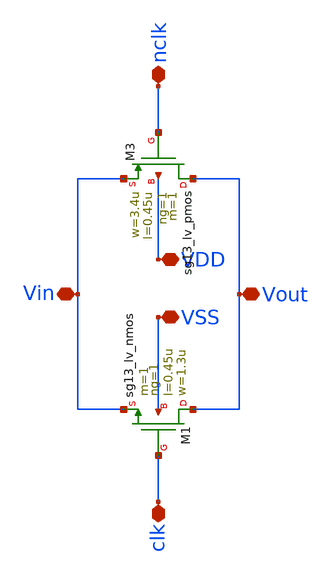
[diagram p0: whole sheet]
** sch_path: unic_cass_wrapper_user_project/ROs_reliability/tgate.sch
**.subckt tgate nclk clk VDD VSS Vout Vin
*.iopin nclk
*.iopin clk
*.iopin VDD
*.iopin VSS
*.iopin Vout
*.iopin Vin
XM3 Vout nclk Vin VDD sg13_lv_pmos w=3.4u l=0.45u ng=1 m=1 mm_ok=1
XM1 Vout clk Vin VSS sg13_lv_nmos w=1.3u l=0.45u ng=1 m=1 mm_ok=1
**.ends
.end
